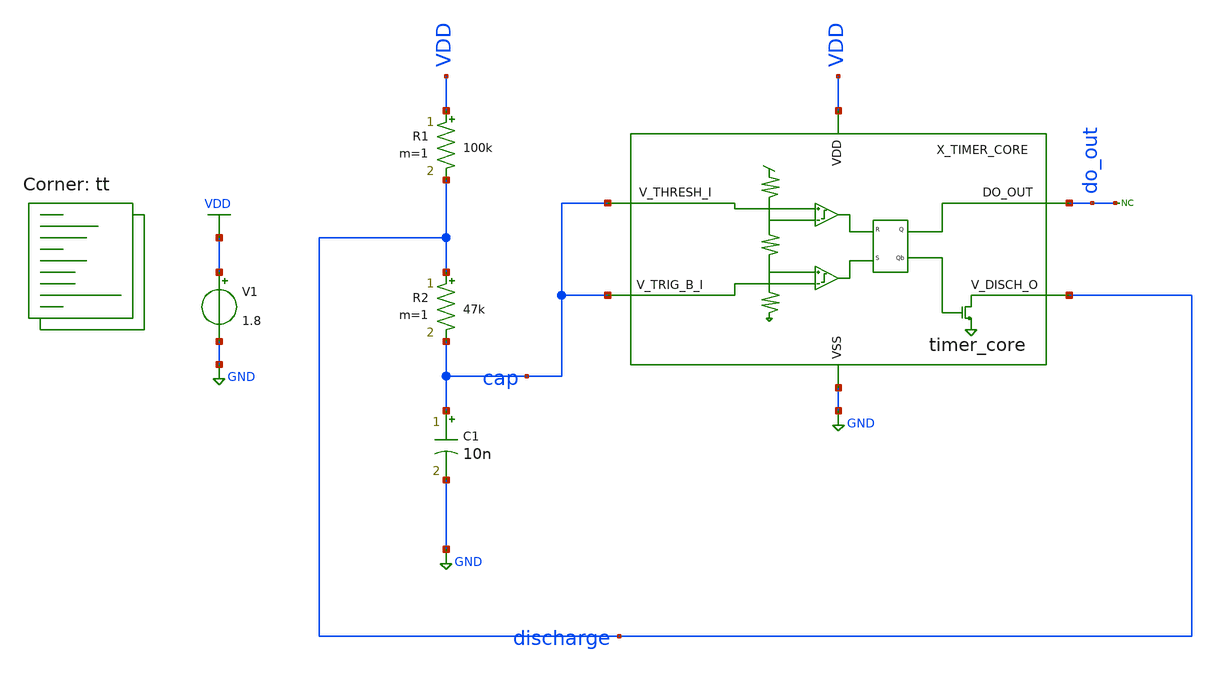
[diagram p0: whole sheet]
** sch_path: xsch/tb/timer_core/tb_timer_core_astable.sch
**.subckt tb_timer_core_astable
V1 VDD GND 1.8
R1 VDD discharge 100k m=1
R2 discharge cap 47k m=1
C1 cap GND 10n m=1
X_TIMER_CORE VDD do_out GND discharge cap cap timer_core
* noconn do_out
**** begin user architecture code


.tran 0.01u 5m


.lib $::SKYWATER_MODELS/sky130.lib.spice tt


.save all

.option method=gear
.option savecurrents


**** end user architecture code
**.ends
.GLOBAL VDD
.GLOBAL GND
.end
